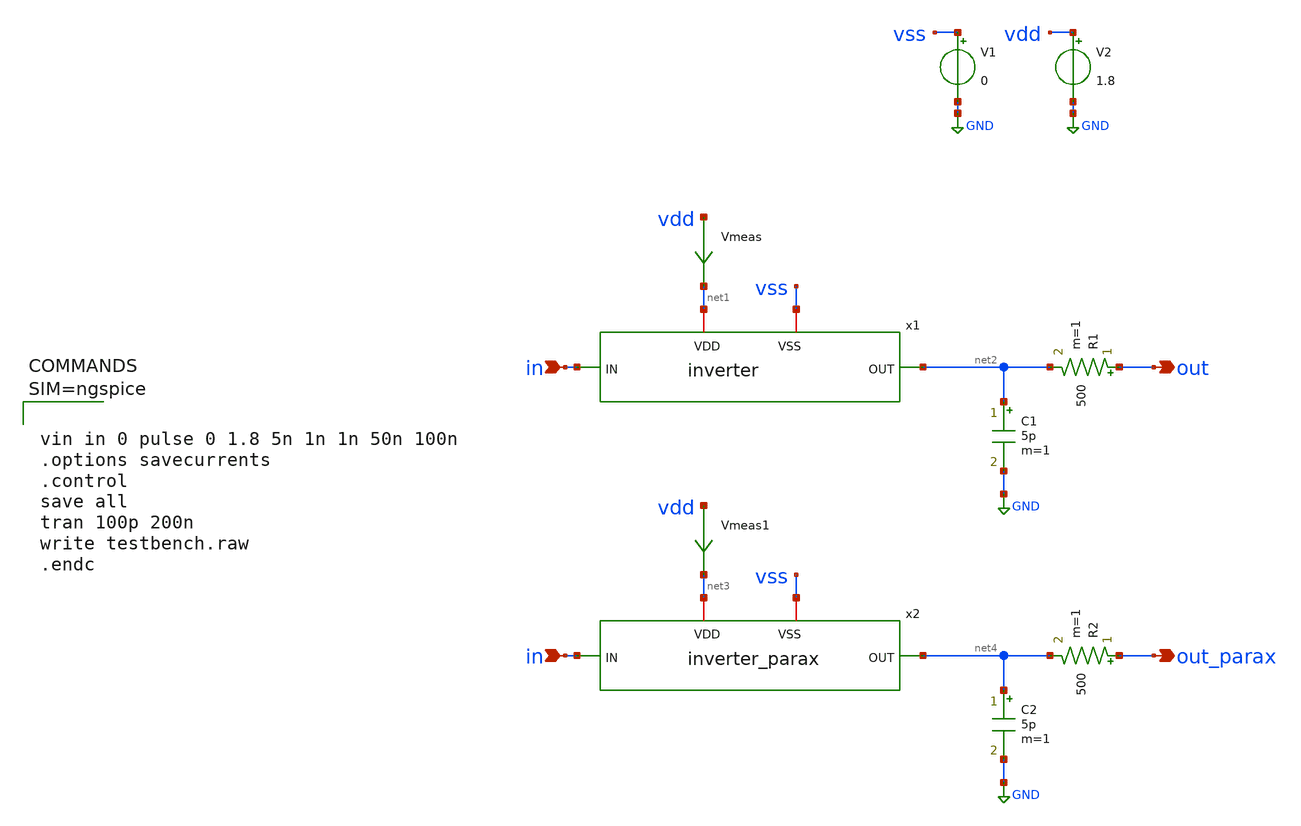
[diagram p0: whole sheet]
** sch_path: xschem/testbench.sch
**.subckt testbench in out in out_parax
*.ipin in
*.opin out
*.ipin in
*.opin out_parax
x1 net1 vss net2 in inverter
V1 vss GND 0
V2 vdd GND 1.8
R1 out net2 500 m=1
C1 net2 GND 5p m=1
Vmeas vdd net1 0
.save i(vmeas)
x2 net3 vss net4 in inverter_parax
R2 out_parax net4 500 m=1
C2 net4 GND 5p m=1
Vmeas1 vdd net3 0
.save i(vmeas1)
**** begin user architecture code

** opencircuitdesign pdks install
.lib $::SKYWATER_MODELS/sky130.lib.spice tt





vin in 0 pulse 0 1.8 5n 1n 1n 50n 100n
.options savecurrents
.control
save all
tran 100p 200n
write testbench.raw
.endc



**** end user architecture code
**.ends

* expanding   symbol:  inverter.sym # of pins=4
** sym_path: xschem/inverter.sym
** sch_path: xschem/inverter.sch
.subckt inverter VDD VSS OUT IN
*.iopin VDD
*.iopin VSS
*.ipin IN
*.opin OUT
XM2 net1 IN VSS VSS sky130_fd_pr__nfet_01v8 L=0.15 W=1 nf=1 ad='int((nf+1)/2) * W/nf * 0.29' as='int((nf+2)/2) * W/nf * 0.29'
+ pd='2*int((nf+1)/2) * (W/nf + 0.29)' ps='2*int((nf+2)/2) * (W/nf + 0.29)' nrd='0.29 / W' nrs='0.29 / W'
+ sa=0 sb=0 sd=0 mult=1 m=1
XM1 net1 IN VDD VDD sky130_fd_pr__pfet_01v8 L=0.15 W=1 nf=1 ad='int((nf+1)/2) * W/nf * 0.29' as='int((nf+2)/2) * W/nf * 0.29'
+ pd='2*int((nf+1)/2) * (W/nf + 0.29)' ps='2*int((nf+2)/2) * (W/nf + 0.29)' nrd='0.29 / W' nrs='0.29 / W'
+ sa=0 sb=0 sd=0 mult=1 m=1
XM3 OUT net1 VSS VSS sky130_fd_pr__nfet_01v8 L=0.15 W=20 nf=20 ad='int((nf+1)/2) * W/nf * 0.29' as='int((nf+2)/2) * W/nf * 0.29'
+ pd='2*int((nf+1)/2) * (W/nf + 0.29)' ps='2*int((nf+2)/2) * (W/nf + 0.29)' nrd='0.29 / W' nrs='0.29 / W'
+ sa=0 sb=0 sd=0 mult=1 m=1
XM4 OUT net1 VDD VDD sky130_fd_pr__pfet_01v8 L=0.15 W=20 nf=20 ad='int((nf+1)/2) * W/nf * 0.29' as='int((nf+2)/2) * W/nf * 0.29'
+ pd='2*int((nf+1)/2) * (W/nf + 0.29)' ps='2*int((nf+2)/2) * (W/nf + 0.29)' nrd='0.29 / W' nrs='0.29 / W'
+ sa=0 sb=0 sd=0 mult=1 m=1
.ends


* expanding   symbol:  inverter_parax.sym # of pins=4
** sym_path: xschem/inverter.sym
.include [file normalize ../mag/inverter.sim.spice]
.GLOBAL GND
.end
